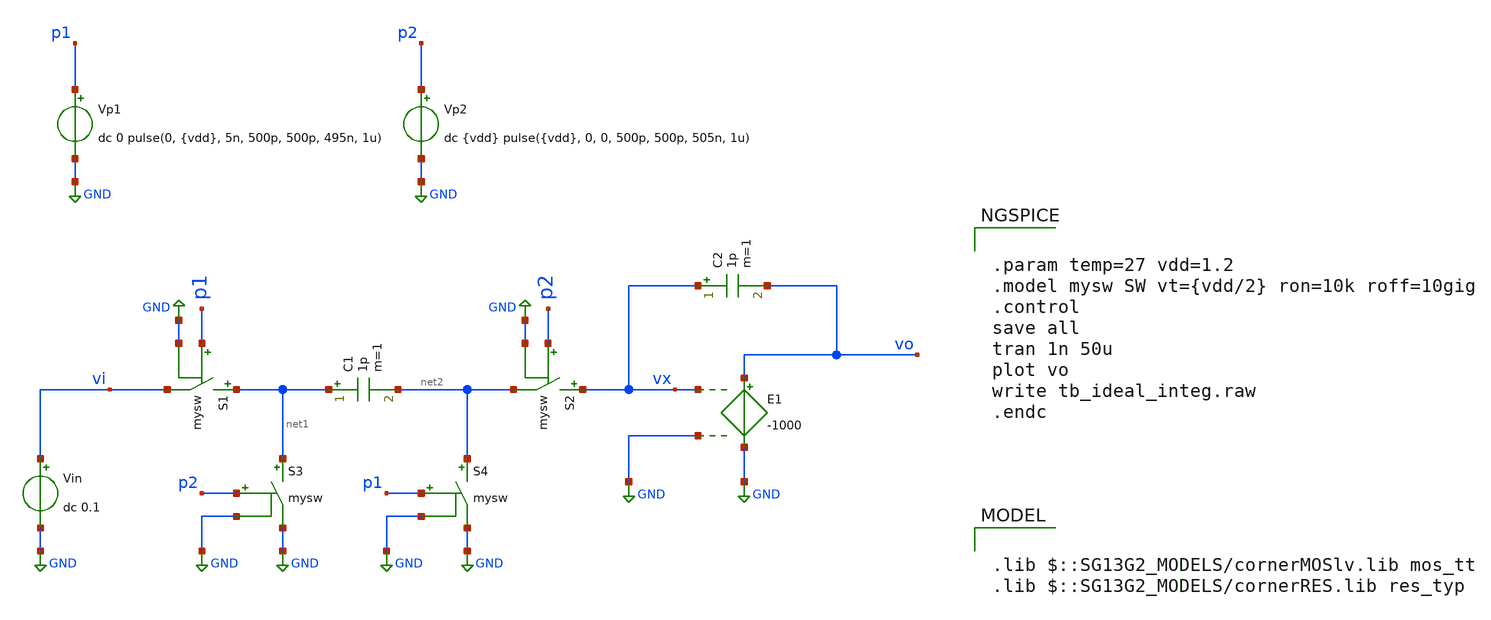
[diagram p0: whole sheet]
** sch_path: 5_Design/2_Idealized_circuits/tb_ideal_integ.sch
**.subckt tb_ideal_integ
Vp1 p1 GND dc 0 pulse(0, {vdd}, 5n, 500p, 500p, 495n, 1u)
E1 vo GND vx GND -1000
S1 net1 vi p1 GND mysw
Vp2 p2 GND dc {vdd} pulse({vdd}, 0, 0, 500p, 500p, 505n, 1u)
Vin vi GND dc 0.1
C1 net1 net2 1p m=1
S2 vx net2 p2 GND mysw
C2 vx vo 1p m=1
S3 net1 GND p2 GND mysw
S4 net2 GND p1 GND mysw
**** begin user architecture code

.lib $::SG13G2_MODELS/cornerMOSlv.lib mos_tt
.lib $::SG13G2_MODELS/cornerRES.lib res_typ



.param temp=27 vdd=1.2
.model mysw SW vt={vdd/2} ron=10k roff=10gig
.control
save all
tran 1n 50u
plot vo
write tb_ideal_integ.raw
.endc


**** end user architecture code
**.ends
.GLOBAL GND
.end
